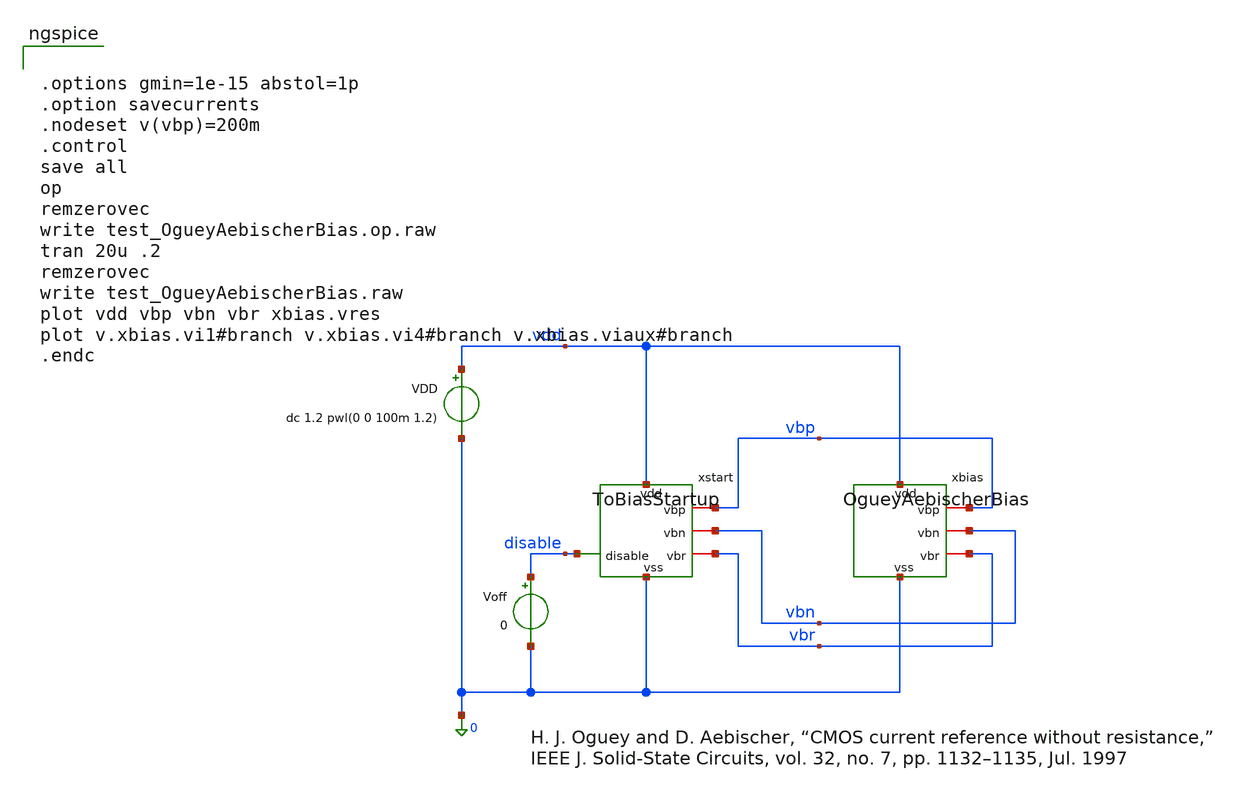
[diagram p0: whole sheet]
** sch_path: macros/OgueyAebischerBias/testbenches/xschem/OgueyAebischerBias_tb.sch
**.subckt OgueyAebischerBias_tb
xbias vdd vbp vbn vbr 0 OgueyAebischerBias
xstart vdd vbp vbn disable vbr 0 ToBiasStartup
VDD vdd 0 dc 1.2 pwl(0 0 100m 1.2)
Voff disable 0 0
**** begin user architecture code


.options gmin=1e-15 abstol=1p
.option savecurrents
.nodeset v(vbp)=200m
.control
save all
op
remzerovec
write test_OgueyAebischerBias.op.raw
tran 20u .2
remzerovec
write test_OgueyAebischerBias.raw
plot vdd vbp vbn vbr xbias.vres
plot v.xbias.vi1#branch v.xbias.vi4#branch v.xbias.viaux#branch
.endc


 .lib cornerMOShv.lib mos_tt

.param mc_mm_switch=0
.param mc_pr_switch=1


**** end user architecture code
**.ends
.end
